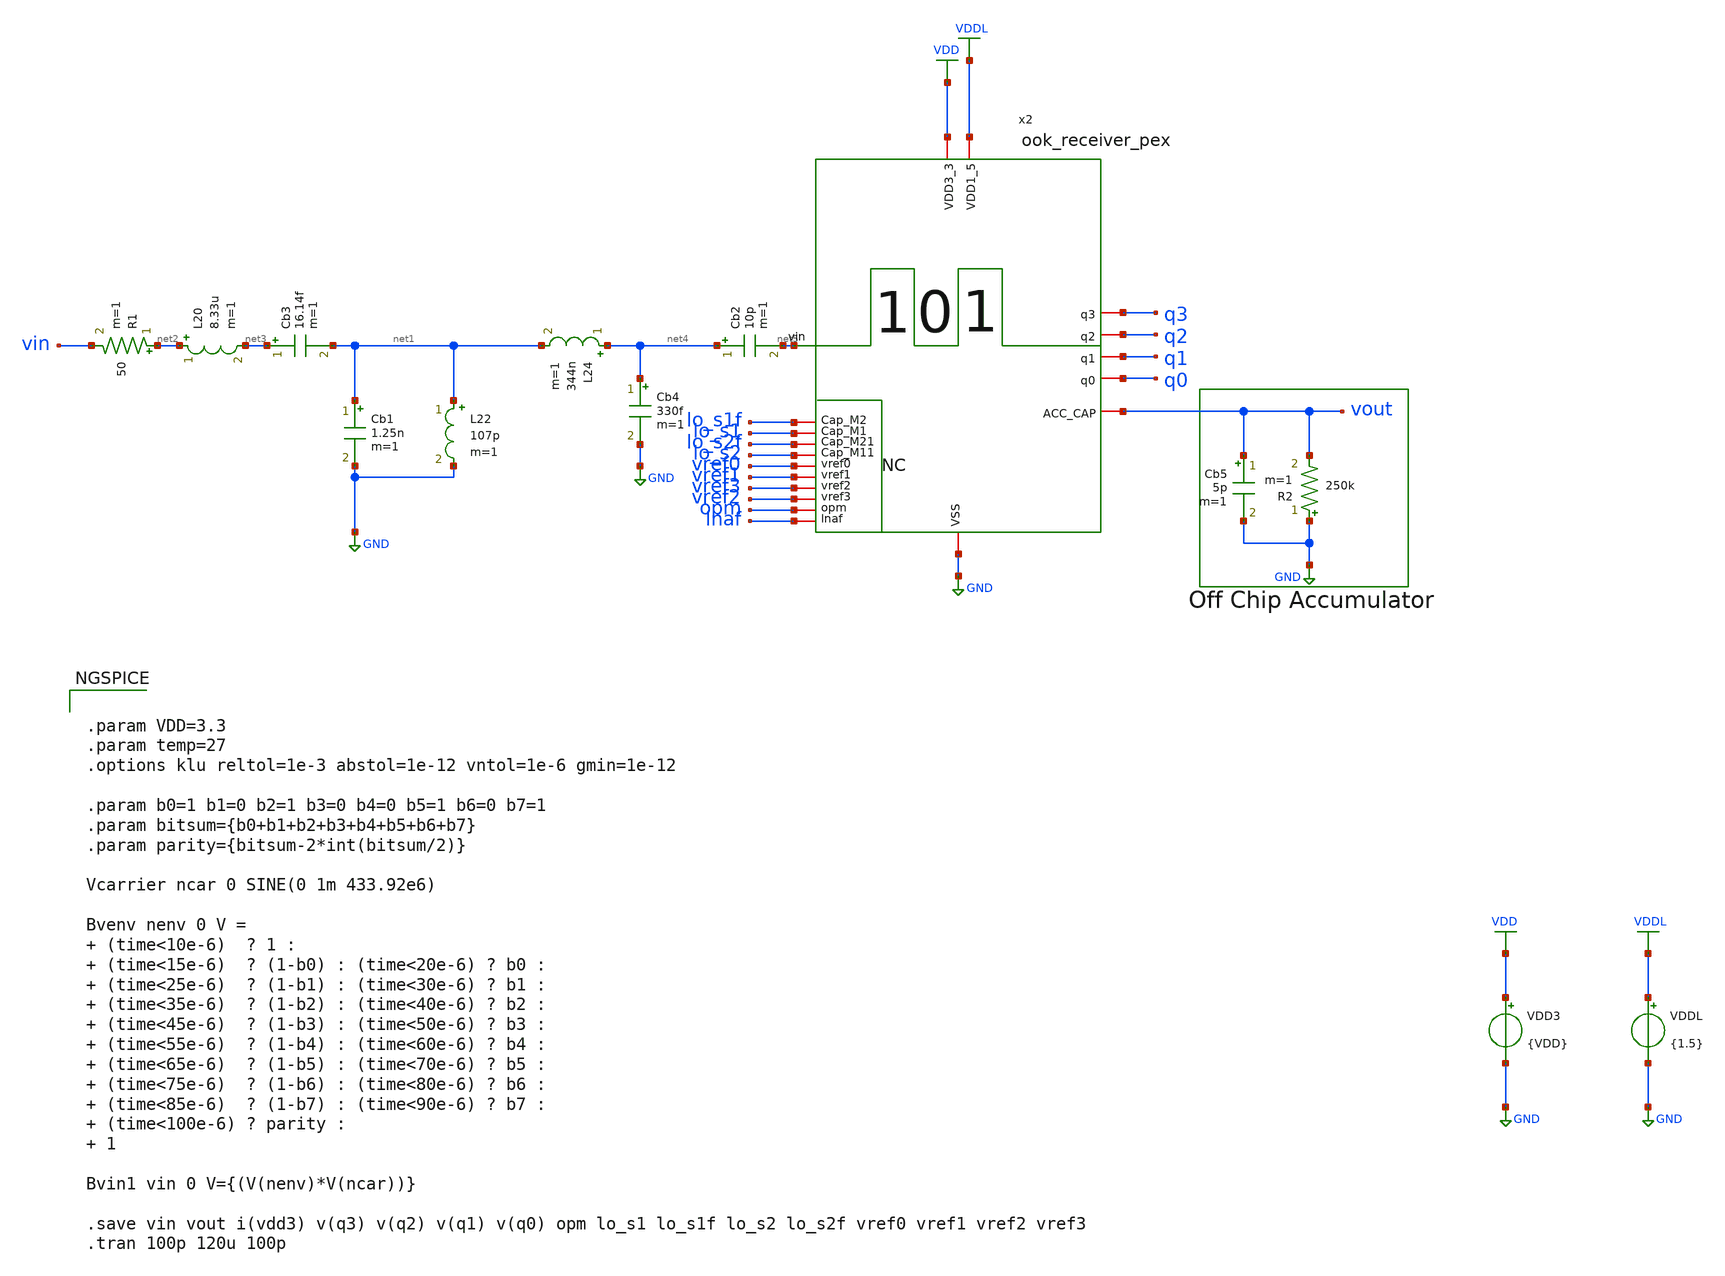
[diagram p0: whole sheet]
** sch_path: macros/heichips26_ook_top/macros/ook_analog_system/testbenches/xschem/ook_receiver_tb_tran.sch
**.subckt ook_receiver_tb_tran
VDD3 VDD GND {VDD}
Cb2 net4 net5 10p m=1
L20 net2 net3 8.33u m=1
R1 net2 vin 50 m=1
Cb1 net1 GND 1.25n m=1
Cb3 net3 net1 16.14f m=1
L22 net1 GND 107p m=1
L24 net4 net1 344n m=1
Cb4 net4 GND 330f m=1
Cb5 vout GND 5p m=1
R2 GND vout 250k m=1
VDDL VDDL GND {1.5}
x2 VDDL opm q0 vref0 q1 vref1 vout q2 vref3 vref2 q3 VDD lo_s2 lo_s2f lo_s1 lo_s1f net5 GND lnaf
+ ook_receiver_pex
**** begin user architecture code


.param VDD=3.3
.param temp=27
.options klu reltol=1e-3 abstol=1e-12 vntol=1e-6 gmin=1e-12

.param b0=1 b1=0 b2=1 b3=0 b4=0 b5=1 b6=0 b7=1
.param bitsum={b0+b1+b2+b3+b4+b5+b6+b7}
.param parity={bitsum-2*int(bitsum/2)}

Vcarrier ncar 0 SINE(0 1m 433.92e6)

Bvenv nenv 0 V =  (time<10e-6)  ? 1 :  (time<15e-6)  ? (1-b0) : (time<20e-6) ? b0 :  (time<25e-6)  ?
+ (1-b1) : (time<30e-6) ? b1 :  (time<35e-6)  ? (1-b2) : (time<40e-6) ? b2 :  (time<45e-6)  ? (1-b3) :
+ (time<50e-6) ? b3 :  (time<55e-6)  ? (1-b4) : (time<60e-6) ? b4 :  (time<65e-6)  ? (1-b5) : (time<70e-6) ? b5 :
+  (time<75e-6)  ? (1-b6) : (time<80e-6) ? b6 :  (time<85e-6)  ? (1-b7) : (time<90e-6) ? b7 :  (time<100e-6) ?
+ parity :  1

Bvin1 vin 0 V={(V(nenv)*V(ncar))}

.save vin vout i(vdd3) v(q3) v(q2) v(q1) v(q0) opm lo_s1 lo_s1f lo_s2 lo_s2f vref0 vref1 vref2 vref3
.tran 100p 120u 100p



.lib cornerMOSlv.lib mos_tt
.lib cornerMOShv.lib mos_tt
.lib cornerRES.lib res_typ
.lib cornerDIO.lib dio_tt
.lib cornerCAP.lib cap_typ
.include /home/belal/HeiChips/heichips26-on-off/IHP-Open-PDK/ihp-sg13cmos5l/libs.tech/ngspice/models/cap_mfringe.lib
.include /home/belal/HeiChips/heichips26-on-off/macros/heichips26_ook_top/macros/ook_analog_system/netlist/pex/ook_receiver_magic_pex_3.spice


**** end user architecture code
**.ends
.GLOBAL GND
.GLOBAL VDD
.GLOBAL VDDL
.end
